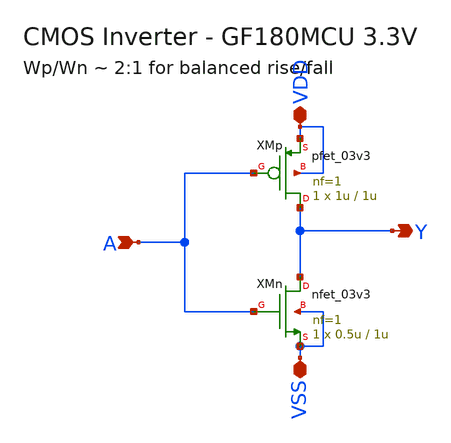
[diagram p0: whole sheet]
** sch_path: designs/libs/core_analog/pfd/leftover_files/inv.sch
**.subckt inv A Y VDD VSS
*.ipin A
*.opin Y
*.iopin VDD
*.iopin VSS
XMp Y A VDD VDD pfet_03v3 L=1u W=1u nf=1 ad='int((nf+1)/2) * W/nf * 0.18u' as='int((nf+2)/2) * W/nf * 0.18u'
+ pd='2*int((nf+1)/2) * (W/nf + 0.18u)' ps='2*int((nf+2)/2) * (W/nf + 0.18u)' nrd='0.18u / W' nrs='0.18u / W'
+ sa=0 sb=0 sd=0 m=1
XMn Y A VSS VSS nfet_03v3 L=1u W=0.5u nf=1 ad='int((nf+1)/2) * W/nf * 0.18u' as='int((nf+2)/2) * W/nf * 0.18u'
+ pd='2*int((nf+1)/2) * (W/nf + 0.18u)' ps='2*int((nf+2)/2) * (W/nf + 0.18u)' nrd='0.18u / W' nrs='0.18u / W'
+ sa=0 sb=0 sd=0 m=1
**.ends
.end
